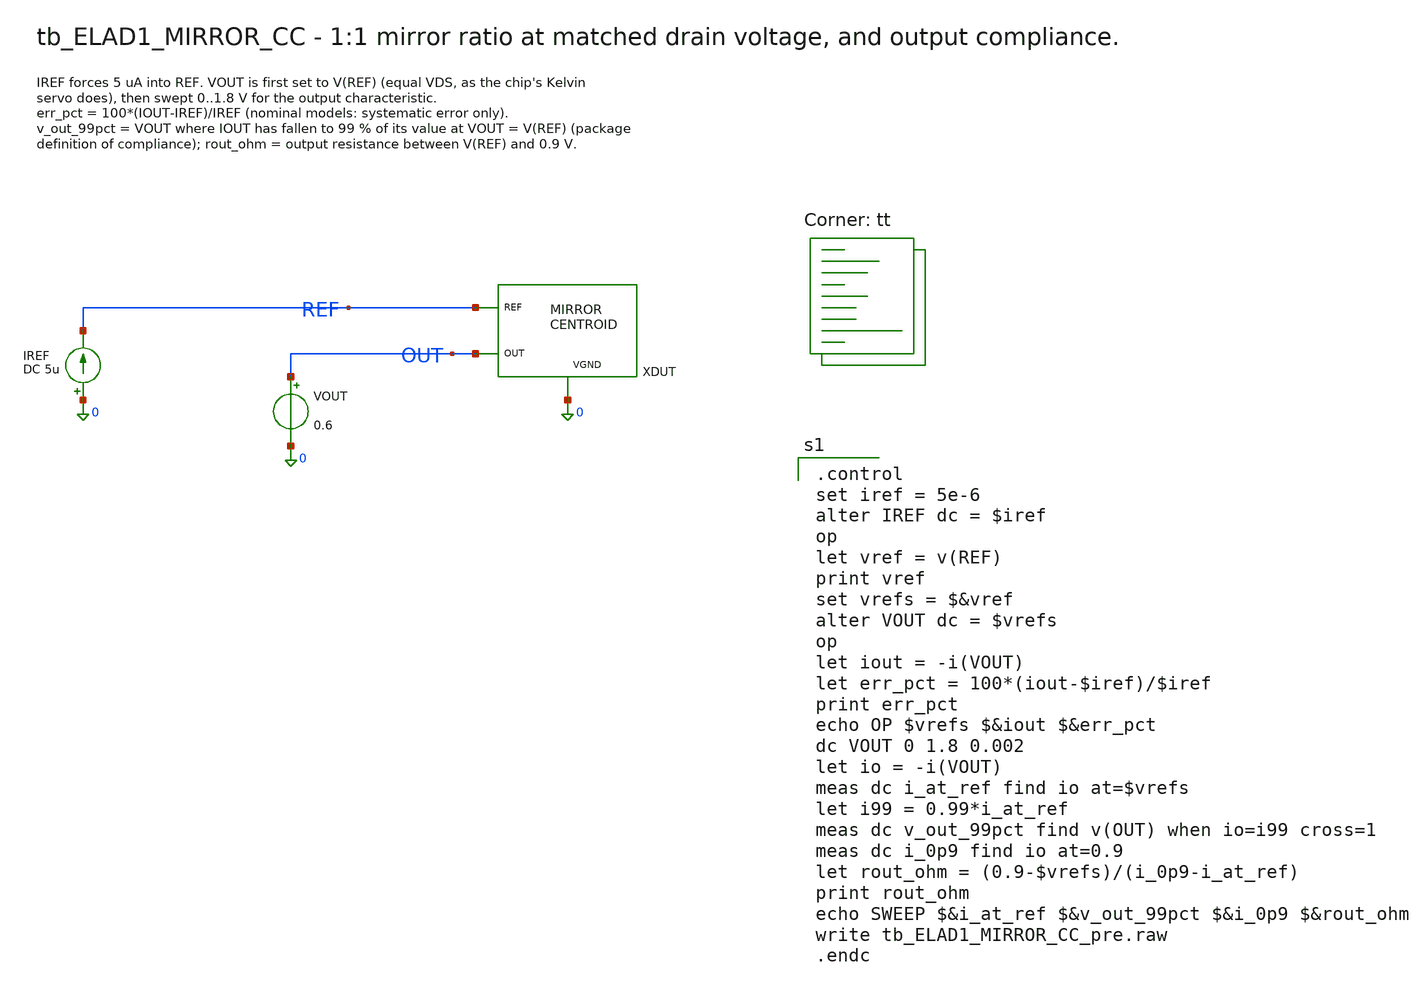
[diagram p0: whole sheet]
** sch_path: cells/ELAD1_MIRROR_CC/schematic/tb_ELAD1_MIRROR_CC.sch
**.subckt tb_ELAD1_MIRROR_CC
XDUT REF OUT 0 ELAD1_MIRROR_CC
VOUT OUT 0 0.6
IREF 0 REF DC 5u
**** begin user architecture code

.control
set iref = 5e-6
alter IREF dc = $iref
op
let vref = v(REF)
print vref
set vrefs = $&vref
alter VOUT dc = $vrefs
op
let iout = -i(VOUT)
let err_pct = 100*(iout-$iref)/$iref
print err_pct
echo OP $vrefs $&iout $&err_pct
dc VOUT 0 1.8 0.002
let io = -i(VOUT)
meas dc i_at_ref find io at=$vrefs
let i99 = 0.99*i_at_ref
meas dc v_out_99pct find v(OUT) when io=i99 cross=1
meas dc i_0p9 find io at=0.9
let rout_ohm = (0.9-$vrefs)/(i_0p9-i_at_ref)
print rout_ohm
echo SWEEP $&i_at_ref $&v_out_99pct $&i_0p9 $&rout_ohm
write tb_ELAD1_MIRROR_CC_pre.raw
.endc

.lib $::SKYWATER_MODELS/sky130.lib.spice tt
**** end user architecture code
**.ends

* expanding   symbol:  ELAD1_MIRROR_CC.sym # of pins=3
** sym_path: cells/ELAD1_MIRROR_CC/schematic/ELAD1_MIRROR_CC.sym
** sch_path: cells/ELAD1_MIRROR_CC/schematic/ELAD1_MIRROR_CC.sch
.subckt ELAD1_MIRROR_CC REF OUT VGND
*.iopin REF
*.iopin OUT
*.iopin VGND
XA[3] REF REF VGND VGND sky130_fd_pr__nfet_01v8 L=1 W=2 nf=1 ad='int((1 + 1)/2) * 2 / 1 * 0.29' as='int((1 + 2)/2) * 2 / 1 * 0.29'
+ pd='2*int((1 + 1)/2) * (2 / 1 + 0.29)' ps='2*int((1 + 2)/2) * (2 / 1 + 0.29)' nrd='0.29 / 2 ' nrs='0.29 / 2 '
+ sa=0 sb=0 sd=0 mult=1 m=1
XA[2] REF REF VGND VGND sky130_fd_pr__nfet_01v8 L=1 W=2 nf=1 ad='int((1 + 1)/2) * 2 / 1 * 0.29' as='int((1 + 2)/2) * 2 / 1 * 0.29'
+ pd='2*int((1 + 1)/2) * (2 / 1 + 0.29)' ps='2*int((1 + 2)/2) * (2 / 1 + 0.29)' nrd='0.29 / 2 ' nrs='0.29 / 2 '
+ sa=0 sb=0 sd=0 mult=1 m=1
XA[1] REF REF VGND VGND sky130_fd_pr__nfet_01v8 L=1 W=2 nf=1 ad='int((1 + 1)/2) * 2 / 1 * 0.29' as='int((1 + 2)/2) * 2 / 1 * 0.29'
+ pd='2*int((1 + 1)/2) * (2 / 1 + 0.29)' ps='2*int((1 + 2)/2) * (2 / 1 + 0.29)' nrd='0.29 / 2 ' nrs='0.29 / 2 '
+ sa=0 sb=0 sd=0 mult=1 m=1
XA[0] REF REF VGND VGND sky130_fd_pr__nfet_01v8 L=1 W=2 nf=1 ad='int((1 + 1)/2) * 2 / 1 * 0.29' as='int((1 + 2)/2) * 2 / 1 * 0.29'
+ pd='2*int((1 + 1)/2) * (2 / 1 + 0.29)' ps='2*int((1 + 2)/2) * (2 / 1 + 0.29)' nrd='0.29 / 2 ' nrs='0.29 / 2 '
+ sa=0 sb=0 sd=0 mult=1 m=1
XB[3] OUT REF VGND VGND sky130_fd_pr__nfet_01v8 L=1 W=2 nf=1 ad='int((1 + 1)/2) * 2 / 1 * 0.29' as='int((1 + 2)/2) * 2 / 1 * 0.29'
+ pd='2*int((1 + 1)/2) * (2 / 1 + 0.29)' ps='2*int((1 + 2)/2) * (2 / 1 + 0.29)' nrd='0.29 / 2 ' nrs='0.29 / 2 '
+ sa=0 sb=0 sd=0 mult=1 m=1
XB[2] OUT REF VGND VGND sky130_fd_pr__nfet_01v8 L=1 W=2 nf=1 ad='int((1 + 1)/2) * 2 / 1 * 0.29' as='int((1 + 2)/2) * 2 / 1 * 0.29'
+ pd='2*int((1 + 1)/2) * (2 / 1 + 0.29)' ps='2*int((1 + 2)/2) * (2 / 1 + 0.29)' nrd='0.29 / 2 ' nrs='0.29 / 2 '
+ sa=0 sb=0 sd=0 mult=1 m=1
XB[1] OUT REF VGND VGND sky130_fd_pr__nfet_01v8 L=1 W=2 nf=1 ad='int((1 + 1)/2) * 2 / 1 * 0.29' as='int((1 + 2)/2) * 2 / 1 * 0.29'
+ pd='2*int((1 + 1)/2) * (2 / 1 + 0.29)' ps='2*int((1 + 2)/2) * (2 / 1 + 0.29)' nrd='0.29 / 2 ' nrs='0.29 / 2 '
+ sa=0 sb=0 sd=0 mult=1 m=1
XB[0] OUT REF VGND VGND sky130_fd_pr__nfet_01v8 L=1 W=2 nf=1 ad='int((1 + 1)/2) * 2 / 1 * 0.29' as='int((1 + 2)/2) * 2 / 1 * 0.29'
+ pd='2*int((1 + 1)/2) * (2 / 1 + 0.29)' ps='2*int((1 + 2)/2) * (2 / 1 + 0.29)' nrd='0.29 / 2 ' nrs='0.29 / 2 '
+ sa=0 sb=0 sd=0 mult=1 m=1
XDUM[15] VGND VGND VGND VGND sky130_fd_pr__nfet_01v8 L=1 W=2 nf=1 ad='int((1 + 1)/2) * 2 / 1 * 0.29'
+ as='int((1 + 2)/2) * 2 / 1 * 0.29' pd='2*int((1 + 1)/2) * (2 / 1 + 0.29)' ps='2*int((1 + 2)/2) * (2 / 1 + 0.29)'
+ nrd='0.29 / 2 ' nrs='0.29 / 2 ' sa=0 sb=0 sd=0 mult=1 m=1
XDUM[14] VGND VGND VGND VGND sky130_fd_pr__nfet_01v8 L=1 W=2 nf=1 ad='int((1 + 1)/2) * 2 / 1 * 0.29'
+ as='int((1 + 2)/2) * 2 / 1 * 0.29' pd='2*int((1 + 1)/2) * (2 / 1 + 0.29)' ps='2*int((1 + 2)/2) * (2 / 1 + 0.29)'
+ nrd='0.29 / 2 ' nrs='0.29 / 2 ' sa=0 sb=0 sd=0 mult=1 m=1
XDUM[13] VGND VGND VGND VGND sky130_fd_pr__nfet_01v8 L=1 W=2 nf=1 ad='int((1 + 1)/2) * 2 / 1 * 0.29'
+ as='int((1 + 2)/2) * 2 / 1 * 0.29' pd='2*int((1 + 1)/2) * (2 / 1 + 0.29)' ps='2*int((1 + 2)/2) * (2 / 1 + 0.29)'
+ nrd='0.29 / 2 ' nrs='0.29 / 2 ' sa=0 sb=0 sd=0 mult=1 m=1
XDUM[12] VGND VGND VGND VGND sky130_fd_pr__nfet_01v8 L=1 W=2 nf=1 ad='int((1 + 1)/2) * 2 / 1 * 0.29'
+ as='int((1 + 2)/2) * 2 / 1 * 0.29' pd='2*int((1 + 1)/2) * (2 / 1 + 0.29)' ps='2*int((1 + 2)/2) * (2 / 1 + 0.29)'
+ nrd='0.29 / 2 ' nrs='0.29 / 2 ' sa=0 sb=0 sd=0 mult=1 m=1
XDUM[11] VGND VGND VGND VGND sky130_fd_pr__nfet_01v8 L=1 W=2 nf=1 ad='int((1 + 1)/2) * 2 / 1 * 0.29'
+ as='int((1 + 2)/2) * 2 / 1 * 0.29' pd='2*int((1 + 1)/2) * (2 / 1 + 0.29)' ps='2*int((1 + 2)/2) * (2 / 1 + 0.29)'
+ nrd='0.29 / 2 ' nrs='0.29 / 2 ' sa=0 sb=0 sd=0 mult=1 m=1
XDUM[10] VGND VGND VGND VGND sky130_fd_pr__nfet_01v8 L=1 W=2 nf=1 ad='int((1 + 1)/2) * 2 / 1 * 0.29'
+ as='int((1 + 2)/2) * 2 / 1 * 0.29' pd='2*int((1 + 1)/2) * (2 / 1 + 0.29)' ps='2*int((1 + 2)/2) * (2 / 1 + 0.29)'
+ nrd='0.29 / 2 ' nrs='0.29 / 2 ' sa=0 sb=0 sd=0 mult=1 m=1
XDUM[9] VGND VGND VGND VGND sky130_fd_pr__nfet_01v8 L=1 W=2 nf=1 ad='int((1 + 1)/2) * 2 / 1 * 0.29' as='int((1 + 2)/2) * 2 / 1 * 0.29'
+ pd='2*int((1 + 1)/2) * (2 / 1 + 0.29)' ps='2*int((1 + 2)/2) * (2 / 1 + 0.29)' nrd='0.29 / 2 ' nrs='0.29 / 2 '
+ sa=0 sb=0 sd=0 mult=1 m=1
XDUM[8] VGND VGND VGND VGND sky130_fd_pr__nfet_01v8 L=1 W=2 nf=1 ad='int((1 + 1)/2) * 2 / 1 * 0.29' as='int((1 + 2)/2) * 2 / 1 * 0.29'
+ pd='2*int((1 + 1)/2) * (2 / 1 + 0.29)' ps='2*int((1 + 2)/2) * (2 / 1 + 0.29)' nrd='0.29 / 2 ' nrs='0.29 / 2 '
+ sa=0 sb=0 sd=0 mult=1 m=1
XDUM[7] VGND VGND VGND VGND sky130_fd_pr__nfet_01v8 L=1 W=2 nf=1 ad='int((1 + 1)/2) * 2 / 1 * 0.29' as='int((1 + 2)/2) * 2 / 1 * 0.29'
+ pd='2*int((1 + 1)/2) * (2 / 1 + 0.29)' ps='2*int((1 + 2)/2) * (2 / 1 + 0.29)' nrd='0.29 / 2 ' nrs='0.29 / 2 '
+ sa=0 sb=0 sd=0 mult=1 m=1
XDUM[6] VGND VGND VGND VGND sky130_fd_pr__nfet_01v8 L=1 W=2 nf=1 ad='int((1 + 1)/2) * 2 / 1 * 0.29' as='int((1 + 2)/2) * 2 / 1 * 0.29'
+ pd='2*int((1 + 1)/2) * (2 / 1 + 0.29)' ps='2*int((1 + 2)/2) * (2 / 1 + 0.29)' nrd='0.29 / 2 ' nrs='0.29 / 2 '
+ sa=0 sb=0 sd=0 mult=1 m=1
XDUM[5] VGND VGND VGND VGND sky130_fd_pr__nfet_01v8 L=1 W=2 nf=1 ad='int((1 + 1)/2) * 2 / 1 * 0.29' as='int((1 + 2)/2) * 2 / 1 * 0.29'
+ pd='2*int((1 + 1)/2) * (2 / 1 + 0.29)' ps='2*int((1 + 2)/2) * (2 / 1 + 0.29)' nrd='0.29 / 2 ' nrs='0.29 / 2 '
+ sa=0 sb=0 sd=0 mult=1 m=1
XDUM[4] VGND VGND VGND VGND sky130_fd_pr__nfet_01v8 L=1 W=2 nf=1 ad='int((1 + 1)/2) * 2 / 1 * 0.29' as='int((1 + 2)/2) * 2 / 1 * 0.29'
+ pd='2*int((1 + 1)/2) * (2 / 1 + 0.29)' ps='2*int((1 + 2)/2) * (2 / 1 + 0.29)' nrd='0.29 / 2 ' nrs='0.29 / 2 '
+ sa=0 sb=0 sd=0 mult=1 m=1
XDUM[3] VGND VGND VGND VGND sky130_fd_pr__nfet_01v8 L=1 W=2 nf=1 ad='int((1 + 1)/2) * 2 / 1 * 0.29' as='int((1 + 2)/2) * 2 / 1 * 0.29'
+ pd='2*int((1 + 1)/2) * (2 / 1 + 0.29)' ps='2*int((1 + 2)/2) * (2 / 1 + 0.29)' nrd='0.29 / 2 ' nrs='0.29 / 2 '
+ sa=0 sb=0 sd=0 mult=1 m=1
XDUM[2] VGND VGND VGND VGND sky130_fd_pr__nfet_01v8 L=1 W=2 nf=1 ad='int((1 + 1)/2) * 2 / 1 * 0.29' as='int((1 + 2)/2) * 2 / 1 * 0.29'
+ pd='2*int((1 + 1)/2) * (2 / 1 + 0.29)' ps='2*int((1 + 2)/2) * (2 / 1 + 0.29)' nrd='0.29 / 2 ' nrs='0.29 / 2 '
+ sa=0 sb=0 sd=0 mult=1 m=1
XDUM[1] VGND VGND VGND VGND sky130_fd_pr__nfet_01v8 L=1 W=2 nf=1 ad='int((1 + 1)/2) * 2 / 1 * 0.29' as='int((1 + 2)/2) * 2 / 1 * 0.29'
+ pd='2*int((1 + 1)/2) * (2 / 1 + 0.29)' ps='2*int((1 + 2)/2) * (2 / 1 + 0.29)' nrd='0.29 / 2 ' nrs='0.29 / 2 '
+ sa=0 sb=0 sd=0 mult=1 m=1
XDUM[0] VGND VGND VGND VGND sky130_fd_pr__nfet_01v8 L=1 W=2 nf=1 ad='int((1 + 1)/2) * 2 / 1 * 0.29' as='int((1 + 2)/2) * 2 / 1 * 0.29'
+ pd='2*int((1 + 1)/2) * (2 / 1 + 0.29)' ps='2*int((1 + 2)/2) * (2 / 1 + 0.29)' nrd='0.29 / 2 ' nrs='0.29 / 2 '
+ sa=0 sb=0 sd=0 mult=1 m=1
.ends

.end
